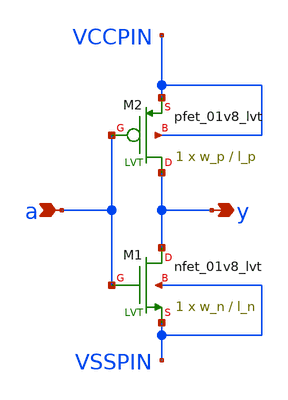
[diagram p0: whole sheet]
** sch_path: sky130_tests_X/lvtnot.sch
* Copyright 2020 Stefan Frederik Schippers
* Licensed under the Apache License, Version 2.0 (the "License");
* you may not use this file except in compliance with the License.
* You may obtain a copy of the License at
* https://www.apache.org/licenses/LICENSE-2.0
* Unless required by applicable law or agreed to in writing, software
* distributed under the License is distributed on an "AS IS" BASIS,
* WITHOUT WARRANTIES OR CONDITIONS OF ANY KIND, either express or implied.
* See the License for the specific language governing permissions and
* limitations under the License.
**.subckt lvtnot y a
*.opin y
*.ipin a
XM2 y a VCCPIN VCCPIN sky130_fd_pr__pfet_01v8_lvt w=w_p l=l_p ad=[sky130_fet_ad_cb w_p ]
+ pd=[sky130_fet_pd_cb w_p ] as=[sky130_fet_ad_cb w_p ] ps=[sky130_fet_pd_cb w_p ] nrd=[sky130_fet_nrd_cb w_p ]
+ nrs=[sky130_fet_nrd_cb w_p ] sa=0 sb=0 sd=0 nf=1 mult=1 m=1
XM1 y a VSSPIN VSSPIN sky130_fd_pr__nfet_01v8_lvt w=w_n l=l_n ad=[sky130_fet_ad_cb w_n ]
+ pd=[sky130_fet_pd_cb w_n ] as=[sky130_fet_ad_cb w_n ] ps=[sky130_fet_pd_cb w_n ] nrd=[sky130_fet_nrd_cb w_n ]
+ nrs=[sky130_fet_nrd_cb w_n ] sa=0 sb=0 sd=0 nf=1 mult=1 m=1
**.ends
.end
